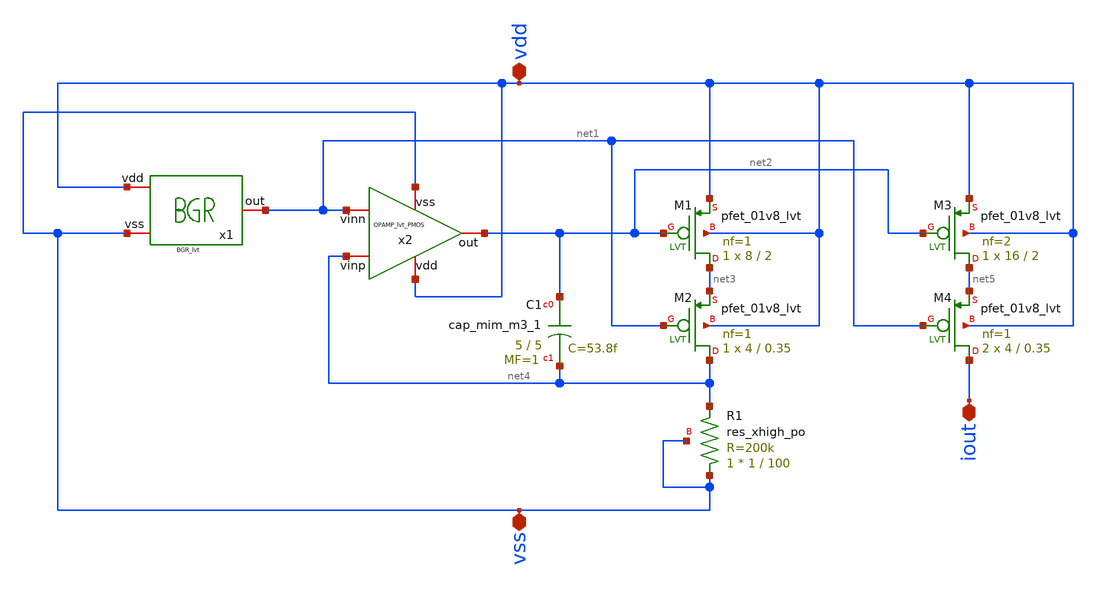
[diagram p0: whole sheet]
** sch_path: ANOTHER_SOLUTIONS_CONSIDERED/ANOTHER_BIAS_FOR_TEMPERATURE_SENSOR/CURRENT_SOURCE_FULL/XSCHEM/current_source.sch
**.subckt current_source vdd vss iout
*.iopin vdd
*.iopin vss
*.iopin iout
XC1 net2 net4 sky130_fd_pr__cap_mim_m3_1 W=5 L=5 MF=1 m=1
XM1 net3 net2 vdd vdd sky130_fd_pr__pfet_01v8_lvt L=2 W=8 nf=1 ad='int((nf+1)/2) * W/nf * 0.29' as='int((nf+2)/2) * W/nf * 0.29'
+ pd='2*int((nf+1)/2) * (W/nf + 0.29)' ps='2*int((nf+2)/2) * (W/nf + 0.29)' nrd='0.29 / W' nrs='0.29 / W'
+ sa=0 sb=0 sd=0 mult=1 m=1
XM2 net4 net1 net3 vdd sky130_fd_pr__pfet_01v8_lvt L=0.35 W=4 nf=1 ad='int((nf+1)/2) * W/nf * 0.29' as='int((nf+2)/2) * W/nf * 0.29'
+ pd='2*int((nf+1)/2) * (W/nf + 0.29)' ps='2*int((nf+2)/2) * (W/nf + 0.29)' nrd='0.29 / W' nrs='0.29 / W'
+ sa=0 sb=0 sd=0 mult=1 m=1
XR1 vss net4 vss sky130_fd_pr__res_xhigh_po W=1 L=100 mult=1 m=1
XM3 net5 net2 vdd vdd sky130_fd_pr__pfet_01v8_lvt L=2 W=16 nf=2 ad='int((nf+1)/2) * W/nf * 0.29' as='int((nf+2)/2) * W/nf * 0.29'
+ pd='2*int((nf+1)/2) * (W/nf + 0.29)' ps='2*int((nf+2)/2) * (W/nf + 0.29)' nrd='0.29 / W' nrs='0.29 / W'
+ sa=0 sb=0 sd=0 mult=1 m=1
XM4 iout net1 net5 vdd sky130_fd_pr__pfet_01v8_lvt L=0.35 W=4 nf=1 ad='int((nf+1)/2) * W/nf * 0.29' as='int((nf+2)/2) * W/nf * 0.29'
+ pd='2*int((nf+1)/2) * (W/nf + 0.29)' ps='2*int((nf+2)/2) * (W/nf + 0.29)' nrd='0.29 / W' nrs='0.29 / W'
+ sa=0 sb=0 sd=0 mult=2 m=2
x1 vdd net1 vss BGR_lvt
x2 vdd net1 net4 net2 vss OPAMP_lvt_PMOS
**.ends
.end
